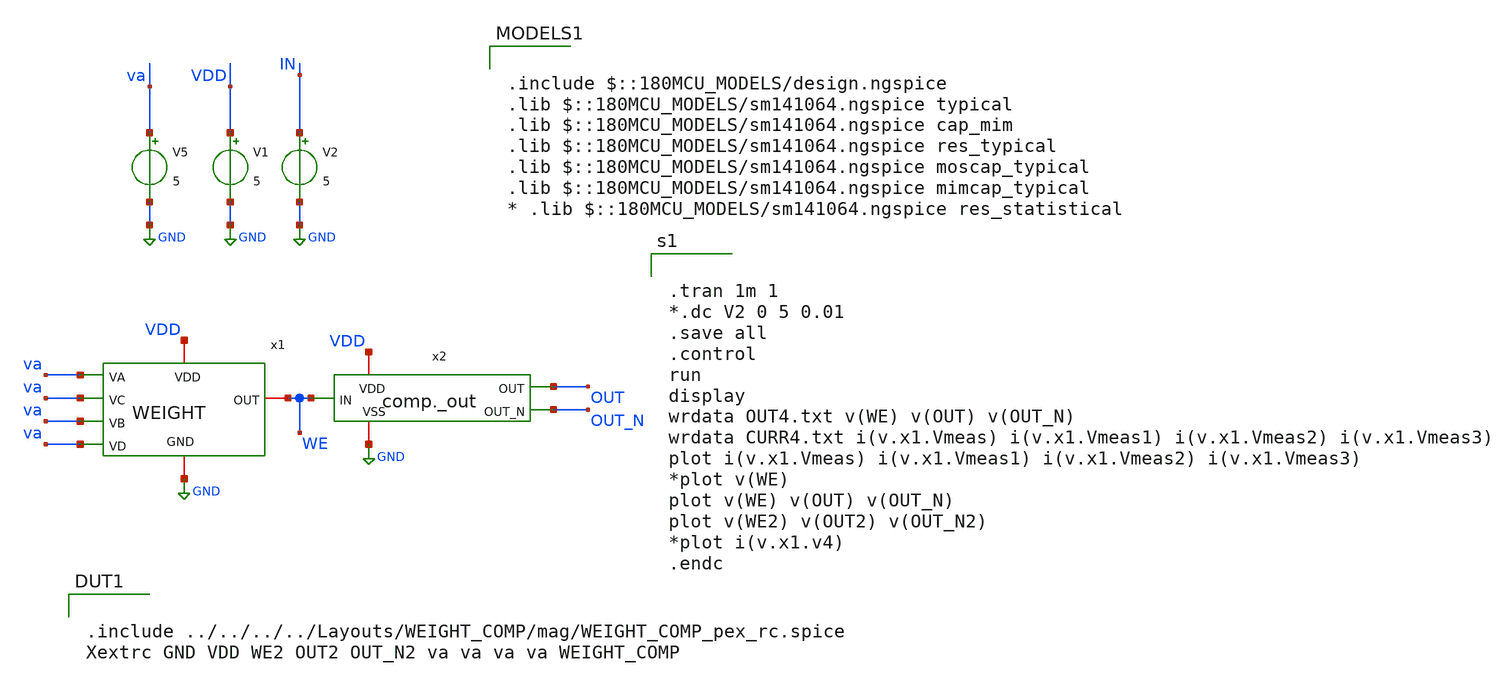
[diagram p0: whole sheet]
** sch_path: FINAL/XSCHEM/TEST/test_weight.sch
**.subckt test_weight
V1 VDD GND 5
V2 IN GND 5
V5 va GND 5
x1 VDD GND WE va va va va WEIGHT
x2 VDD OUT WE OUT_N GND comp._out
**** begin user architecture code


.tran 1m 1
*.dc V2 0 5 0.01
.save all
.control
run
display
wrdata OUT4.txt v(WE) v(OUT) v(OUT_N)
wrdata CURR4.txt i(v.x1.Vmeas) i(v.x1.Vmeas1) i(v.x1.Vmeas2) i(v.x1.Vmeas3)
plot i(v.x1.Vmeas) i(v.x1.Vmeas1) i(v.x1.Vmeas2) i(v.x1.Vmeas3)
*plot v(WE)
plot v(WE) v(OUT) v(OUT_N)
plot v(WE2) v(OUT2) v(OUT_N2)
*plot i(v.x1.v4)
.endc



.include $::180MCU_MODELS/design.ngspice
.lib $::180MCU_MODELS/sm141064.ngspice typical
.lib $::180MCU_MODELS/sm141064.ngspice cap_mim
.lib $::180MCU_MODELS/sm141064.ngspice res_typical
.lib $::180MCU_MODELS/sm141064.ngspice moscap_typical
.lib $::180MCU_MODELS/sm141064.ngspice mimcap_typical
* .lib $::180MCU_MODELS/sm141064.ngspice res_statistical


.include ../../../../Layouts/WEIGHT_COMP/mag/WEIGHT_COMP_pex_rc.spice
Xextrc GND VDD WE2 OUT2 OUT_N2 va va va va WEIGHT_COMP



**** end user architecture code
**.ends
.GLOBAL GND
.end
